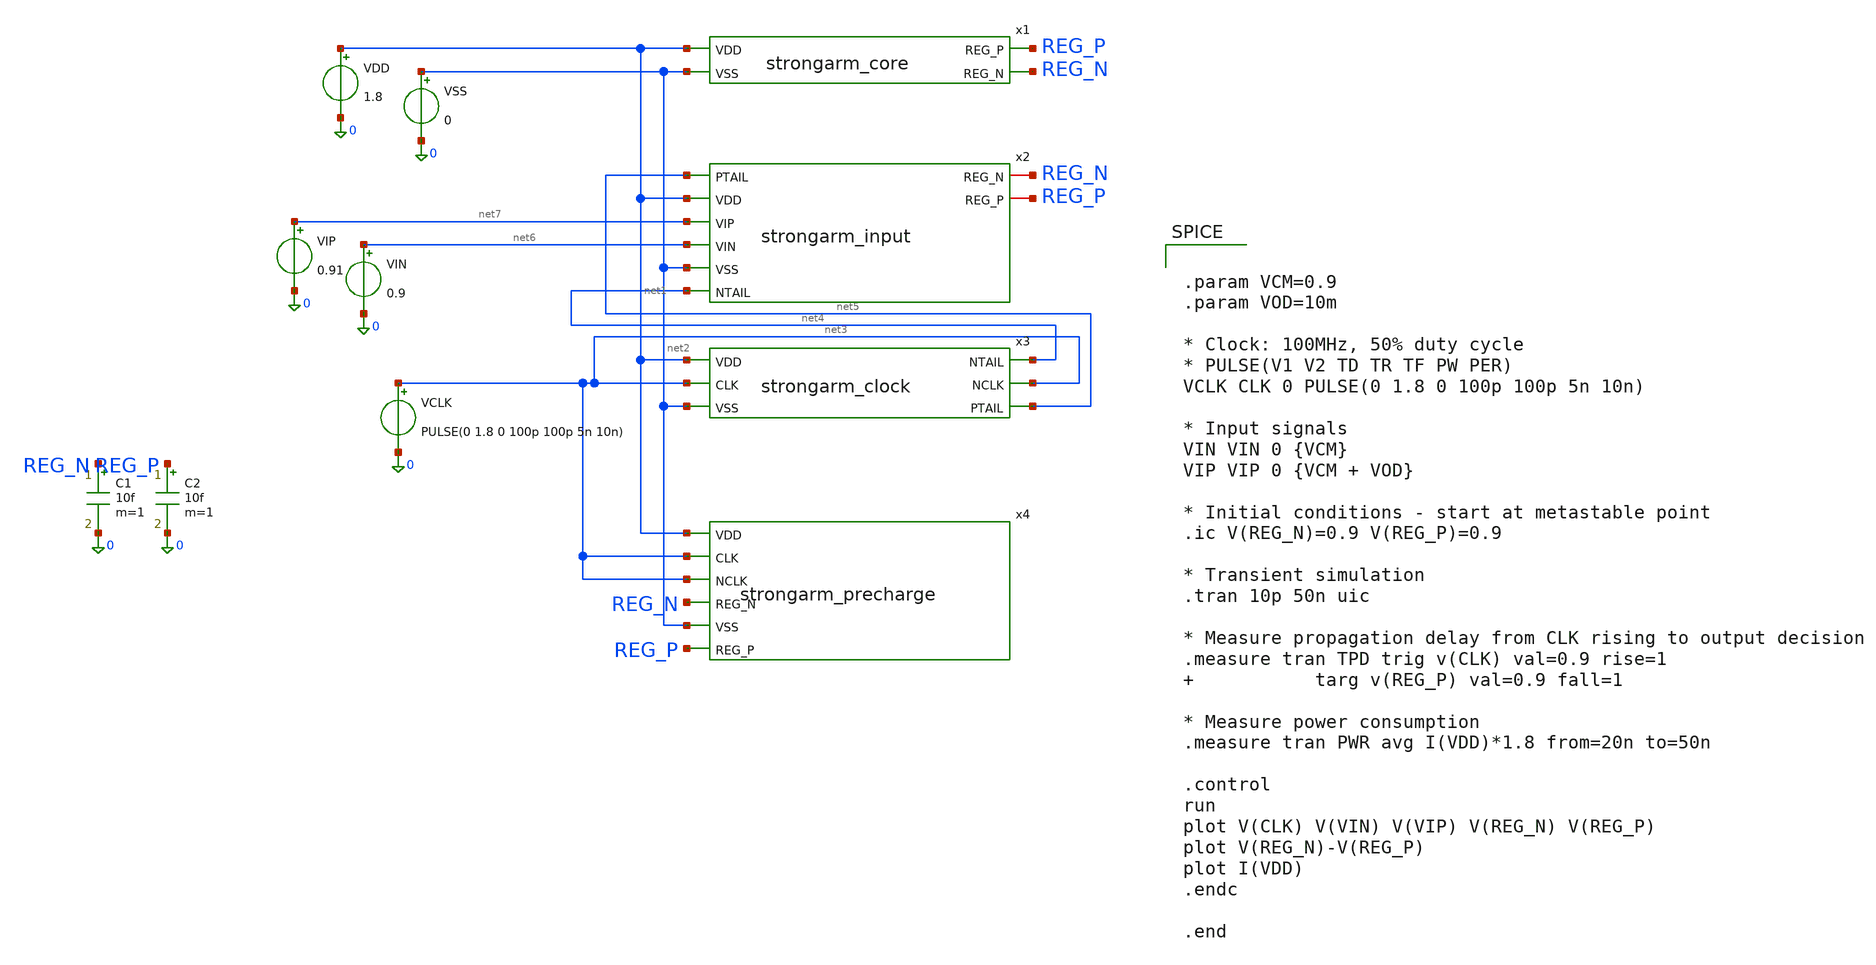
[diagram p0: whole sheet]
** sch_path: tb_comp_clocked.sch
**.subckt tb_comp_clocked
x1 net1 REG_P REG_N net2 strongarm_core
x2 net5 net1 REG_N REG_P net7 net6 net2 net4 strongarm_input
VDD net1 0 1.8
VSS net2 0 0
VIN net6 0 0.9
VIP net7 0 0.91
VCLK net3 0 PULSE(0 1.8 0 100p 100p 5n 10n)
C1 REG_N 0 10f m=1
C2 REG_P 0 10f m=1
x4 net1 net3 net3 REG_N net2 REG_P strongarm_precharge
x3 net4 net1 net3 net3 net5 net2 strongarm_clock
**** begin user architecture code


.param VCM=0.9
.param VOD=10m

* Clock: 100MHz, 50% duty cycle
* PULSE(V1 V2 TD TR TF PW PER)
VCLK CLK 0 PULSE(0 1.8 0 100p 100p 5n 10n)

* Input signals
VIN VIN 0 {VCM}
VIP VIP 0 {VCM + VOD}

* Initial conditions - start at metastable point
.ic V(REG_N)=0.9 V(REG_P)=0.9

* Transient simulation
.tran 10p 50n uic

* Measure propagation delay from CLK rising to output decision
.measure tran TPD trig v(CLK) val=0.9 rise=1             targ v(REG_P) val=0.9 fall=1

* Measure power consumption
.measure tran PWR avg I(VDD)*1.8 from=20n to=50n

.control
run
plot V(CLK) V(VIN) V(VIP) V(REG_N) V(REG_P)
plot V(REG_N)-V(REG_P)
plot I(VDD)
.endc

.end

**** end user architecture code
**.ends

* expanding   symbol:  /home/master/Documents/6_bit_Flash_ADC/strongarm_core.sym # of pins=4
** sym_path: strongarm_core.sym
** sch_path: strongarm_core.sch
.subckt strongarm_core VDD REG_P REG_N VSS
*.ipin VDD
*.ipin VSS
*.opin REG_P
*.opin REG_N
XM8 REG_P REG_N VDD VDD sky130_fd_pr__pfet_01v8 L=0.15 W=12 nf=1 ad='int((1 + 1)/2) * 12 / 1 * 0.29'
+ as='int((1 + 2)/2) * 12 / 1 * 0.29' pd='2*int((1 + 1)/2) * (12 / 1 + 0.29)' ps='2*int((1 + 2)/2) * (12 / 1 + 0.29)'
+ nrd='0.29 / 12 ' nrs='0.29 / 12 ' sa=0 sb=0 sd=0 mult=1 m=1
XM6 REG_P REG_N VSS VSS sky130_fd_pr__nfet_01v8 L=0.15 W=6 nf=1 ad='int((1 + 1)/2) * 6 / 1 * 0.29' as='int((1 + 2)/2) * 6 / 1 * 0.29'
+ pd='2*int((1 + 1)/2) * (6 / 1 + 0.29)' ps='2*int((1 + 2)/2) * (6 / 1 + 0.29)' nrd='0.29 / 6 ' nrs='0.29 / 6 '
+ sa=0 sb=0 sd=0 mult=1 m=1
XM5 REG_N REG_P VSS VSS sky130_fd_pr__nfet_01v8 L=0.15 W=6 nf=1 ad='int((1 + 1)/2) * 6 / 1 * 0.29' as='int((1 + 2)/2) * 6 / 1 * 0.29'
+ pd='2*int((1 + 1)/2) * (6 / 1 + 0.29)' ps='2*int((1 + 2)/2) * (6 / 1 + 0.29)' nrd='0.29 / 6 ' nrs='0.29 / 6 '
+ sa=0 sb=0 sd=0 mult=1 m=1
XM7 REG_N REG_P VDD VDD sky130_fd_pr__pfet_01v8 L=0.15 W=12 nf=1 ad='int((1 + 1)/2) * 12 / 1 * 0.29'
+ as='int((1 + 2)/2) * 12 / 1 * 0.29' pd='2*int((1 + 1)/2) * (12 / 1 + 0.29)' ps='2*int((1 + 2)/2) * (12 / 1 + 0.29)'
+ nrd='0.29 / 12 ' nrs='0.29 / 12 ' sa=0 sb=0 sd=0 mult=1 m=1
.ends


* expanding   symbol:  /home/master/Documents/6_bit_Flash_ADC/strongarm_input.sym # of pins=8
** sym_path: strongarm_input.sym
** sch_path: strongarm_input.sch
.subckt strongarm_input PTAIL VDD REG_N REG_P VIP VIN VSS NTAIL
*.ipin PTAIL
*.ipin NTAIL
*.iopin REG_P
*.iopin REG_N
*.ipin VSS
*.ipin VDD
*.ipin VIP
*.ipin VIN
XM1 REG_N VIN NTAIL VSS sky130_fd_pr__nfet_01v8 L=0.15 W=12 nf=2 ad='int((2 + 1)/2) * 12 / 2 * 0.29'
+ as='int((2 + 2)/2) * 12 / 2 * 0.29' pd='2*int((2 + 1)/2) * (12 / 2 + 0.29)' ps='2*int((2 + 2)/2) * (12 / 2 + 0.29)'
+ nrd='0.29 / 12 ' nrs='0.29 / 12 ' sa=0 sb=0 sd=0 mult=1 m=1
XM2 REG_P VIP NTAIL VSS sky130_fd_pr__nfet_01v8 L=0.15 W=12 nf=2 ad='int((2 + 1)/2) * 12 / 2 * 0.29'
+ as='int((2 + 2)/2) * 12 / 2 * 0.29' pd='2*int((2 + 1)/2) * (12 / 2 + 0.29)' ps='2*int((2 + 2)/2) * (12 / 2 + 0.29)'
+ nrd='0.29 / 12 ' nrs='0.29 / 12 ' sa=0 sb=0 sd=0 mult=1 m=1
XM3 REG_N VIN PTAIL VDD sky130_fd_pr__pfet_01v8 L=0.15 W=24 nf=2 ad='int((2 + 1)/2) * 24 / 2 * 0.29'
+ as='int((2 + 2)/2) * 24 / 2 * 0.29' pd='2*int((2 + 1)/2) * (24 / 2 + 0.29)' ps='2*int((2 + 2)/2) * (24 / 2 + 0.29)'
+ nrd='0.29 / 24 ' nrs='0.29 / 24 ' sa=0 sb=0 sd=0 mult=1 m=1
XM4 REG_P VIP PTAIL VDD sky130_fd_pr__pfet_01v8 L=0.15 W=24 nf=2 ad='int((2 + 1)/2) * 24 / 2 * 0.29'
+ as='int((2 + 2)/2) * 24 / 2 * 0.29' pd='2*int((2 + 1)/2) * (24 / 2 + 0.29)' ps='2*int((2 + 2)/2) * (24 / 2 + 0.29)'
+ nrd='0.29 / 24 ' nrs='0.29 / 24 ' sa=0 sb=0 sd=0 mult=1 m=1
.ends


* expanding   symbol:  /home/master/Documents/6_bit_Flash_ADC/strongarm_precharge.sym # of pins=6
** sym_path: strongarm_precharge.sym
** sch_path: strongarm_precharge.sch
.subckt strongarm_precharge VDD CLK NCLK REG_N VSS REG_P
*.ipin CLK
*.ipin NCLK
*.ipin REG_N
*.ipin REG_P
*.ipin VDD
*.ipin VSS
XMP1 REG_N NCLK VDD VDD sky130_fd_pr__pfet_01v8 L=0.15 W=2 nf=1 ad='int((1 + 1)/2) * 2 / 1 * 0.29' as='int((1 + 2)/2) * 2 / 1 * 0.29'
+ pd='2*int((1 + 1)/2) * (2 / 1 + 0.29)' ps='2*int((1 + 2)/2) * (2 / 1 + 0.29)' nrd='0.29 / 2 ' nrs='0.29 / 2 '
+ sa=0 sb=0 sd=0 mult=1 m=1
XMP2 REG_P NCLK VDD VDD sky130_fd_pr__pfet_01v8 L=0.15 W=2 nf=1 ad='int((1 + 1)/2) * 2 / 1 * 0.29' as='int((1 + 2)/2) * 2 / 1 * 0.29'
+ pd='2*int((1 + 1)/2) * (2 / 1 + 0.29)' ps='2*int((1 + 2)/2) * (2 / 1 + 0.29)' nrd='0.29 / 2 ' nrs='0.29 / 2 '
+ sa=0 sb=0 sd=0 mult=1 m=1
XMN1 REG_N CLK VSS VSS sky130_fd_pr__nfet_01v8 L=0.15 W=1 nf=1 ad='int((1 + 1)/2) * 1 / 1 * 0.29' as='int((1 + 2)/2) * 1 / 1 * 0.29'
+ pd='2*int((1 + 1)/2) * (1 / 1 + 0.29)' ps='2*int((1 + 2)/2) * (1 / 1 + 0.29)' nrd='0.29 / 1 ' nrs='0.29 / 1 '
+ sa=0 sb=0 sd=0 mult=1 m=1
XMN2 REG_P CLK VSS VSS sky130_fd_pr__nfet_01v8 L=0.15 W=1 nf=1 ad='int((1 + 1)/2) * 1 / 1 * 0.29' as='int((1 + 2)/2) * 1 / 1 * 0.29'
+ pd='2*int((1 + 1)/2) * (1 / 1 + 0.29)' ps='2*int((1 + 2)/2) * (1 / 1 + 0.29)' nrd='0.29 / 1 ' nrs='0.29 / 1 '
+ sa=0 sb=0 sd=0 mult=1 m=1
.ends


* expanding   symbol:  /home/master/Documents/6_bit_Flash_ADC/strongarm_clock.sym # of pins=6
** sym_path: strongarm_clock.sym
** sch_path: strongarm_clock.sch
.subckt strongarm_clock NTAIL VDD NCLK CLK PTAIL VSS
*.ipin CLK
*.opin NCLK
*.opin NTAIL
*.opin PTAIL
*.ipin VDD
*.ipin VSS
XM10 PTAIL NCLK VDD VDD sky130_fd_pr__pfet_01v8 L=0.15 W=32 nf=4 ad='int((4 + 1)/2) * 32 / 4 * 0.29'
+ as='int((4 + 2)/2) * 32 / 4 * 0.29' pd='2*int((4 + 1)/2) * (32 / 4 + 0.29)' ps='2*int((4 + 2)/2) * (32 / 4 + 0.29)'
+ nrd='0.29 / 32 ' nrs='0.29 / 32 ' sa=0 sb=0 sd=0 mult=1 m=1
XM9 NTAIL CLK VSS VSS sky130_fd_pr__nfet_01v8 L=0.15 W=16 nf=4 ad='int((4 + 1)/2) * 16 / 4 * 0.29' as='int((4 + 2)/2) * 16 / 4 * 0.29'
+ pd='2*int((4 + 1)/2) * (16 / 4 + 0.29)' ps='2*int((4 + 2)/2) * (16 / 4 + 0.29)' nrd='0.29 / 16 ' nrs='0.29 / 16 '
+ sa=0 sb=0 sd=0 mult=1 m=1
XMp NCLK CLK VDD VDD sky130_fd_pr__pfet_01v8 L=0.15 W=4 nf=1 ad='int((1 + 1)/2) * 4 / 1 * 0.29' as='int((1 + 2)/2) * 4 / 1 * 0.29'
+ pd='2*int((1 + 1)/2) * (4 / 1 + 0.29)' ps='2*int((1 + 2)/2) * (4 / 1 + 0.29)' nrd='0.29 / 4 ' nrs='0.29 / 4 '
+ sa=0 sb=0 sd=0 mult=1 m=1
XMn NCLK CLK VSS VSS sky130_fd_pr__nfet_01v8 L=0.15 W=2 nf=1 ad='int((1 + 1)/2) * 2 / 1 * 0.29' as='int((1 + 2)/2) * 2 / 1 * 0.29'
+ pd='2*int((1 + 1)/2) * (2 / 1 + 0.29)' ps='2*int((1 + 2)/2) * (2 / 1 + 0.29)' nrd='0.29 / 2 ' nrs='0.29 / 2 '
+ sa=0 sb=0 sd=0 mult=1 m=1
.ends

.end
